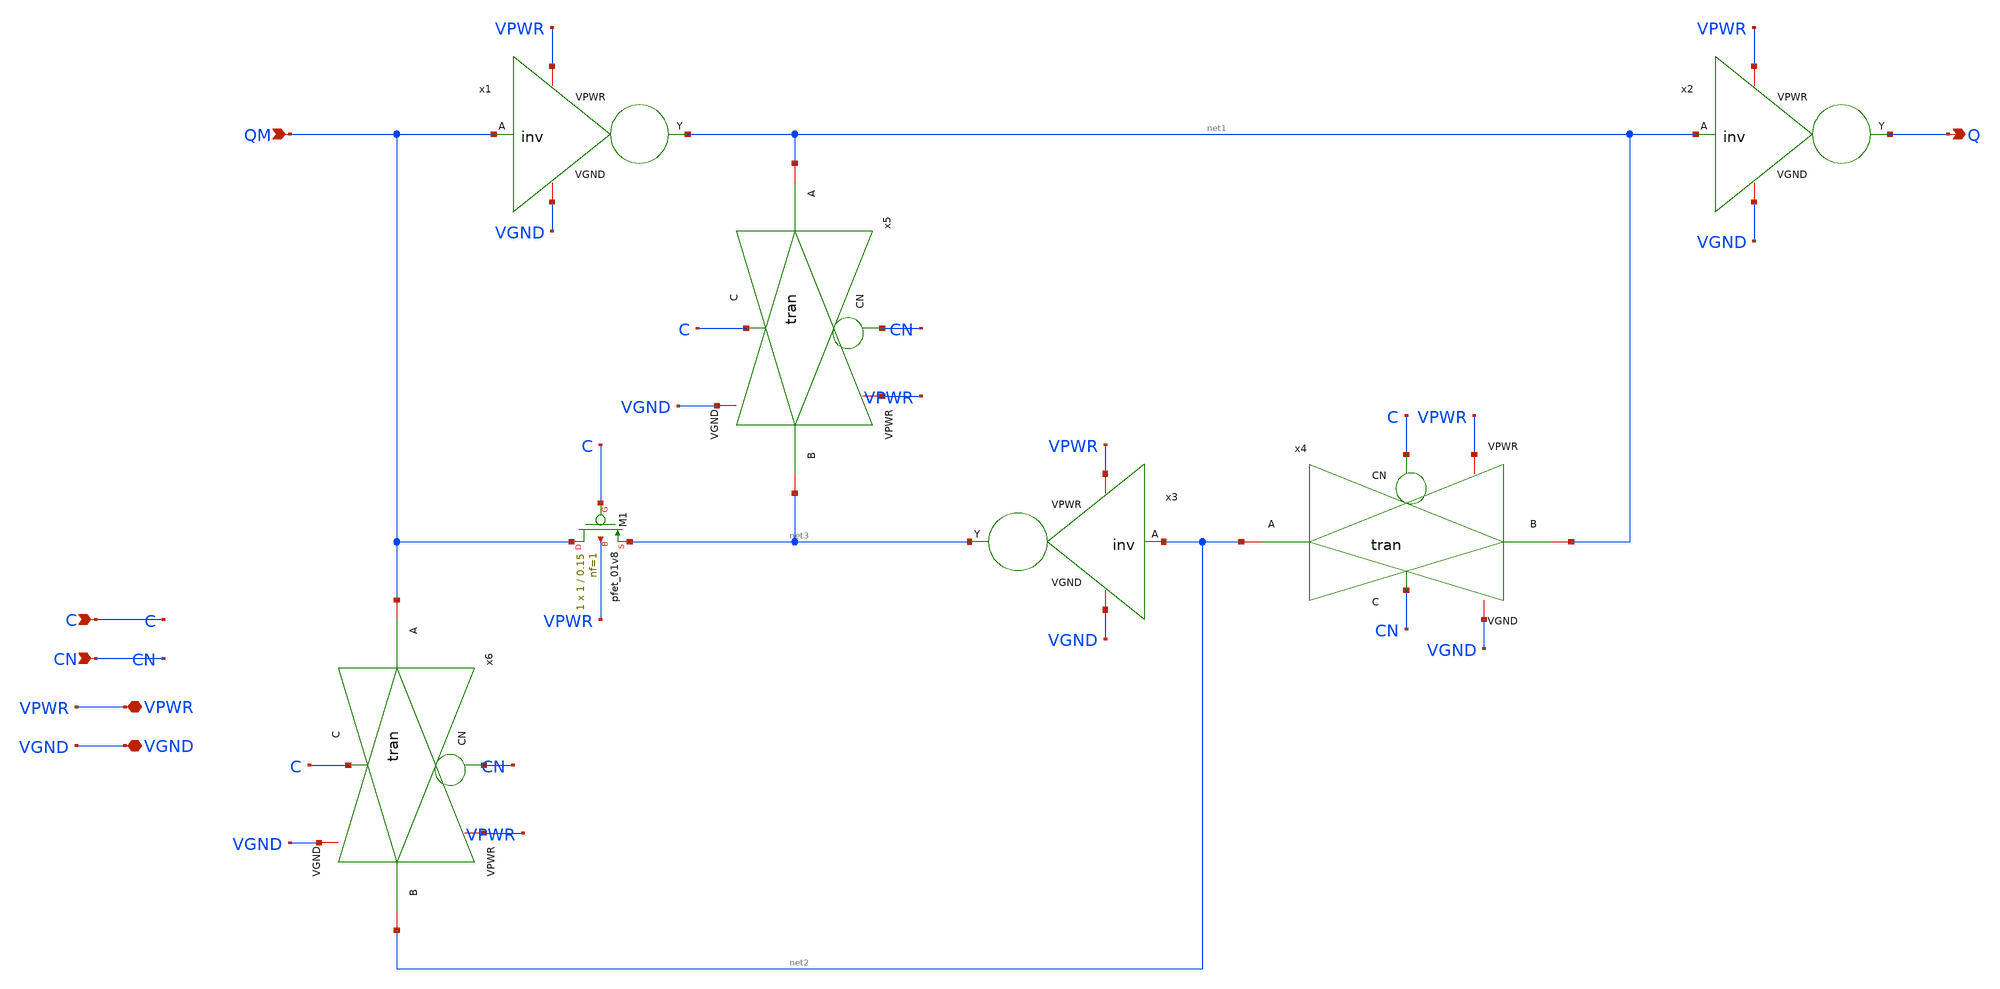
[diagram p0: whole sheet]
** sch_path: slaveLatch/SlaveLatch.sch
**.subckt SlaveLatch C CN VPWR VGND QM Q
*.ipin C
*.ipin CN
*.iopin VPWR
*.iopin VGND
*.ipin QM
*.opin Q
x1 VPWR QM net1 VGND inv
x2 VPWR net1 Q VGND inv
x3 VPWR net2 net3 VGND inv
x4 C VPWR net1 net2 VGND CN tran
x5 CN VPWR net3 net1 VGND C tran
XM1 QM C net3 VPWR sky130_fd_pr__pfet_01v8 L=0.15 W=1 nf=1 ad='int((1 + 1)/2) * 1 / 1 * 0.29' as='int((1 + 2)/2) * 1 / 1 * 0.29'
+ pd='2*int((1 + 1)/2) * (1 / 1 + 0.29)' ps='2*int((1 + 2)/2) * (1 / 1 + 0.29)' nrd='0.29 / 1 ' nrs='0.29 / 1 '
+ sa=0 sb=0 sd=0 mult=1 m=1
x6 CN VPWR net2 QM VGND C tran
**.ends
.end
